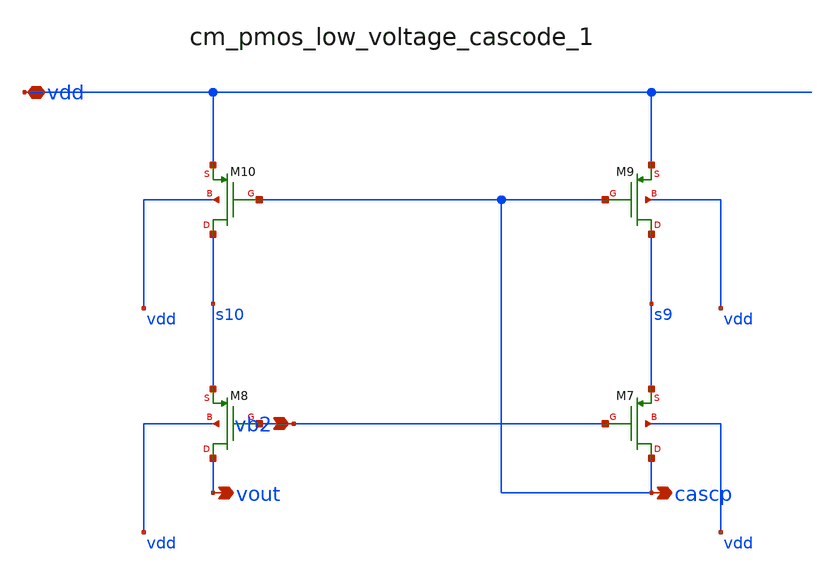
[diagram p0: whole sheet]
** sch_path: analog-db/raw/amp_004_folded_cascode/hier/blocks/cm_pmos_low_voltage_cascode_1.sch
**.subckt cm_pmos_low_voltage_cascode_1 vb2 vdd cascp vout
*.ipin vb2
*.iopin vdd
*.opin cascp
*.opin vout
XM10 s10 cascp vdd vdd sg13_lv_pmos w=x_dut_xm10_w l=x_dut_xm10_l ng=x_dut_xm10_ng m=x_dut_xm10_m
XM7 cascp vb2 s9 vdd sg13_lv_pmos w=x_dut_xm7_w l=x_dut_xm7_l ng=x_dut_xm7_ng m=x_dut_xm7_m
XM8 vout vb2 s10 vdd sg13_lv_pmos w=x_dut_xm8_w l=x_dut_xm8_l ng=x_dut_xm8_ng m=x_dut_xm8_m
XM9 s9 cascp vdd vdd sg13_lv_pmos w=x_dut_xm9_w l=x_dut_xm9_l ng=x_dut_xm9_ng m=x_dut_xm9_m
**.ends
.end
